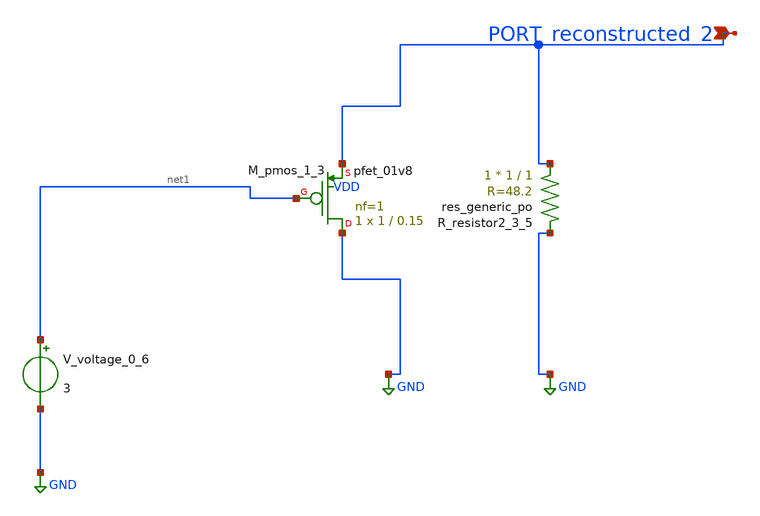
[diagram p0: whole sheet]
** sch_path: schematics/AMSNet/116.sch
**.subckt 116 PORT_reconstructed_2
*.ipin PORT_reconstructed_2
XM_pmos_1_3 GND net1 PORT_reconstructed_2 VDD sky130_fd_pr__pfet_01v8 L=0.15 W=1 nf=1 ad='int((1 + 1)/2) * 1 / 1 * 0.29'
+ as='int((1 + 2)/2) * 1 / 1 * 0.29' pd='2*int((1 + 1)/2) * (1 / 1 + 0.29)' ps='2*int((1 + 2)/2) * (1 / 1 + 0.29)'
+ nrd='0.29 / 1 ' nrs='0.29 / 1 ' sa=0 sb=0 sd=0 mult=1 m=1
XR_resistor2_3_5 PORT_reconstructed_2 GND sky130_fd_pr__res_generic_po W=1 L=1 m=1
V_voltage_0_6 net1 GND 3
**.ends
.GLOBAL GND
.end
